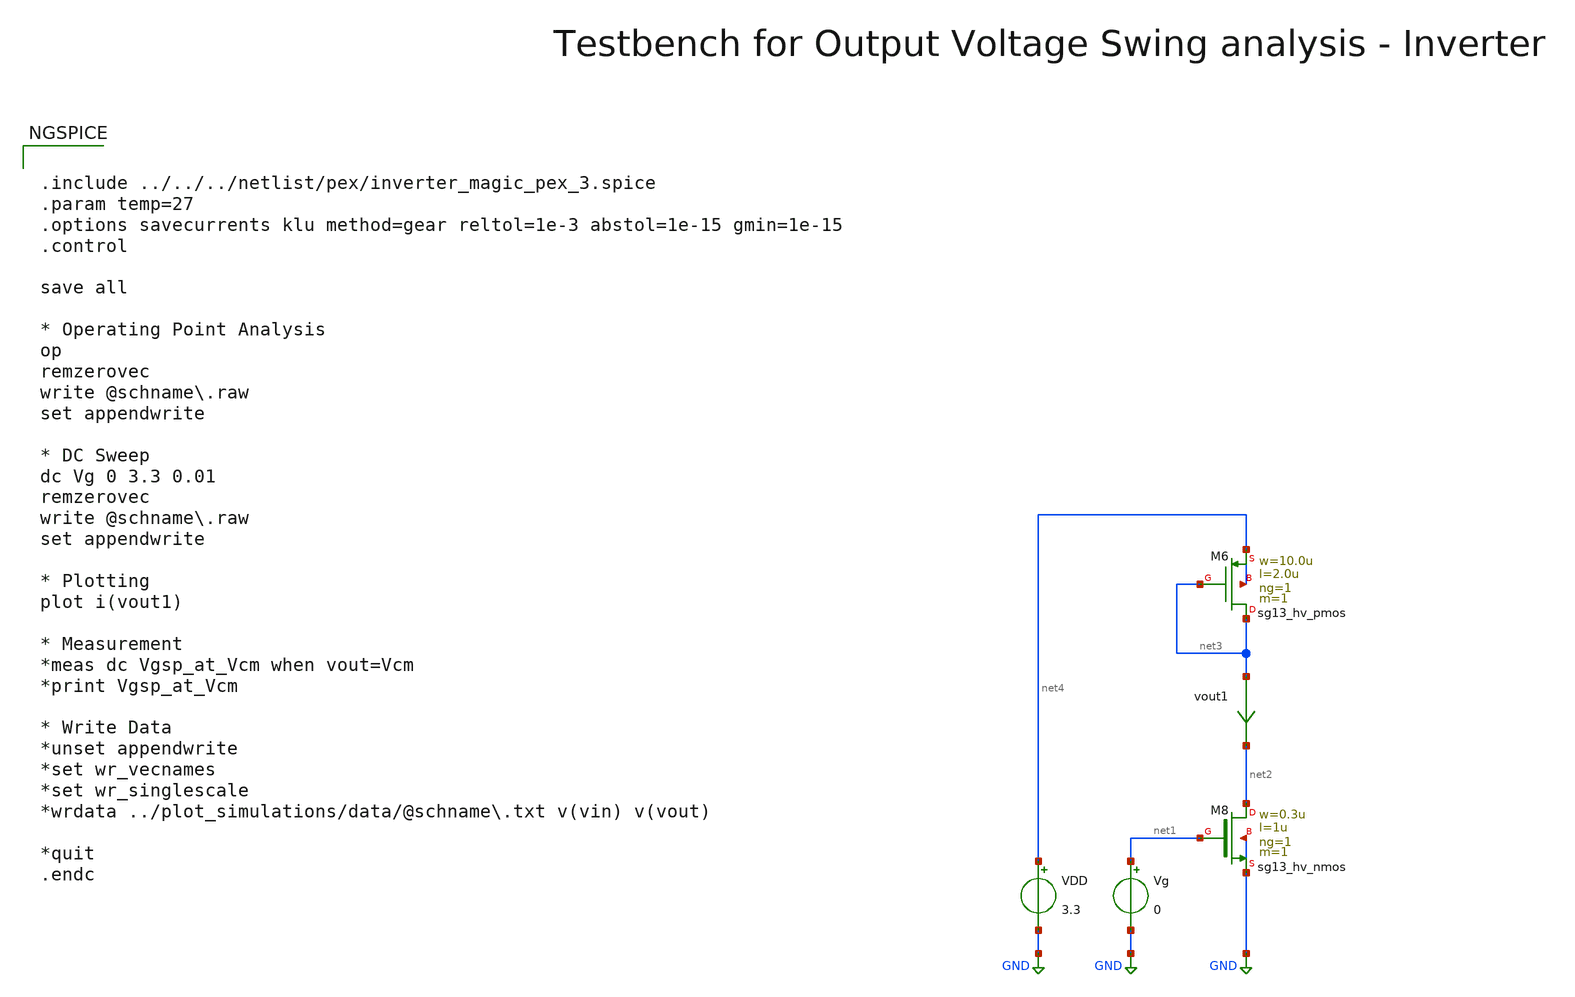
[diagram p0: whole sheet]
** sch_path: macros/heichips26_vcr/macros/switched_capacitor/testbenches/xschem/tb_v-to-i_dc.sch
**.subckt tb_v-to-i_dc
VDD net4 GND 3.3
Vg net1 GND 0
vout1 net3 net2 0
.save i(vout1)
XM8 net2 net1 GND GND sg13_hv_nmos w=0.3u l=1u ng=1 m=1 mm_ok=1
XM6 net3 net3 net4 net4 sg13_hv_pmos w=10.0u l=2.0u ng=1 m=1 mm_ok=1
**** begin user architecture code


.include ../../../netlist/pex/inverter_magic_pex_3.spice
.param temp=27
.options savecurrents klu method=gear reltol=1e-3 abstol=1e-15 gmin=1e-15
.control

save all

* Operating Point Analysis
op
remzerovec
write @schname\.raw
set appendwrite

* DC Sweep
dc Vg 0 3.3 0.01
remzerovec
write @schname\.raw
set appendwrite

* Plotting
plot i(vout1)

* Measurement
*meas dc Vgsp_at_Vcm when vout=Vcm
*print Vgsp_at_Vcm

* Write Data
*unset appendwrite
*set wr_vecnames
*set wr_singlescale
*wrdata ../plot_simulations/data/@schname\.txt v(vin) v(vout)

*quit
.endc



.lib cornerMOSlv.lib mos_tt
.lib cornerMOShv.lib mos_tt
.lib cornerRES.lib res_typ
.lib cornerDIO.lib dio_tt

**** end user architecture code
**.ends
.GLOBAL GND
.end
